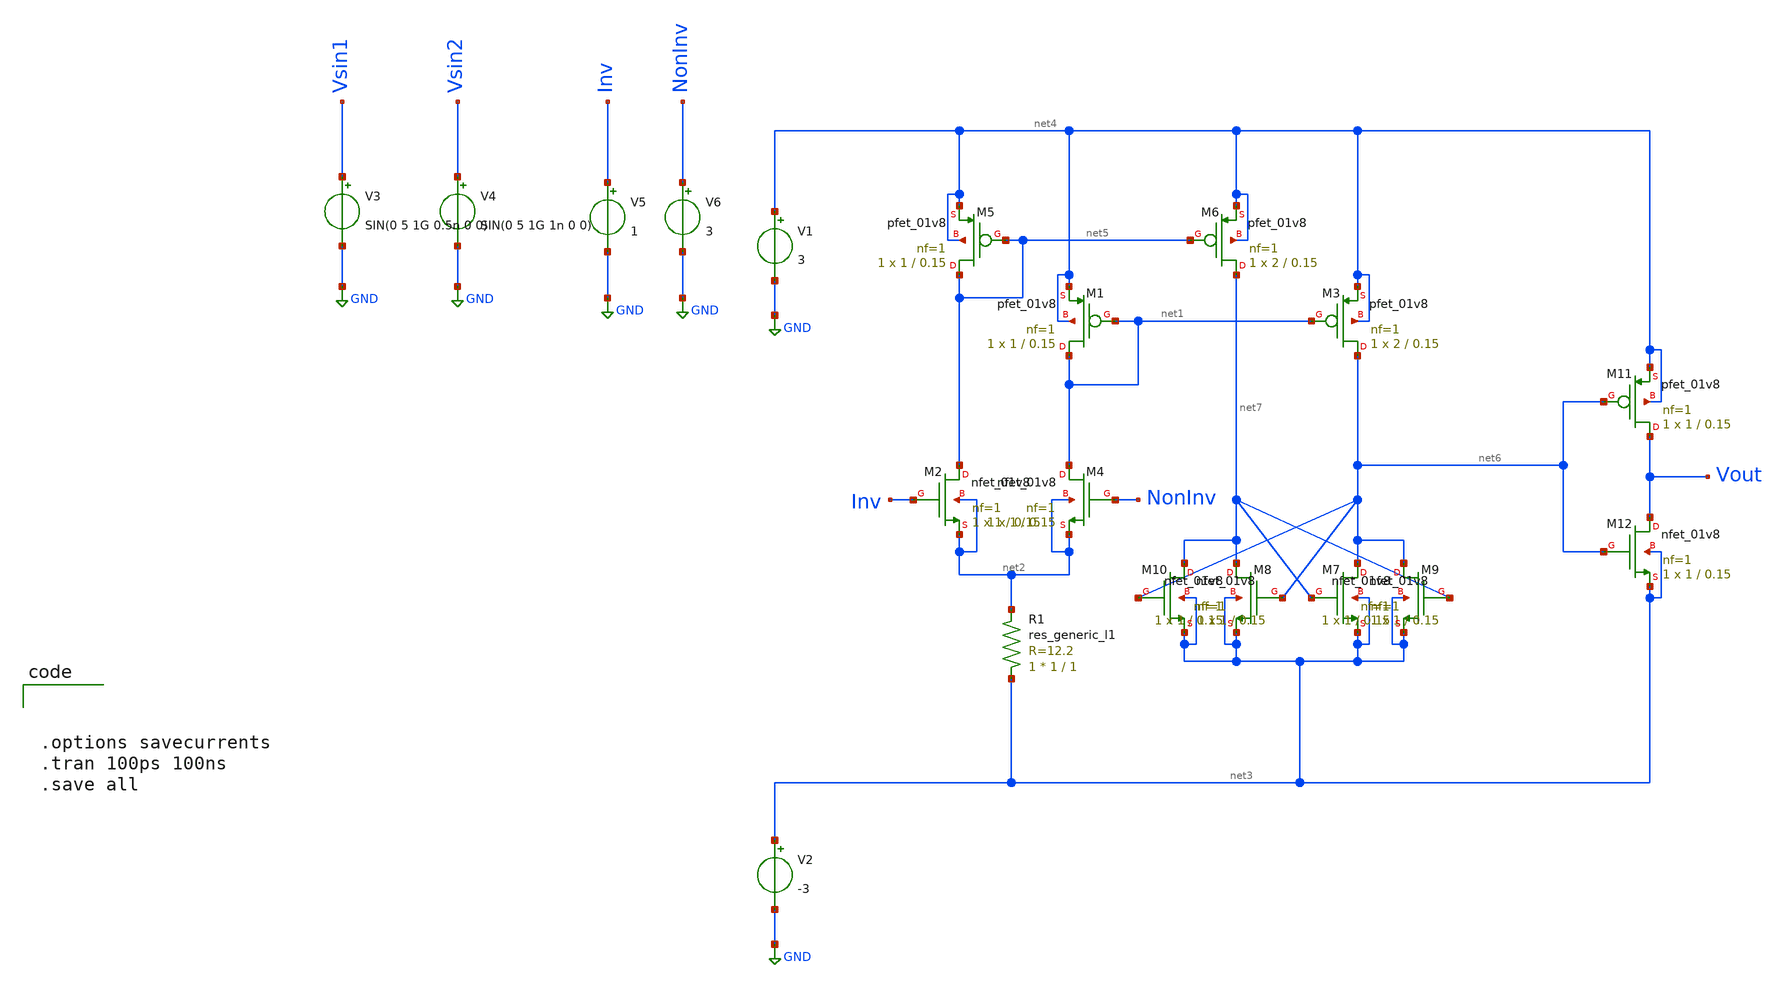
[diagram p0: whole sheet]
** sch_path: Sky130 xsch magic/xscheme/mos_comparator.sch
**.subckt mos_comparator
XM1 net1 net1 net4 net4 sky130_fd_pr__pfet_01v8 L=0.15 W=1 nf=1 ad='int((nf+1)/2) * W/nf * 0.29' as='int((nf+2)/2) * W/nf * 0.29'
+ pd='2*int((nf+1)/2) * (W/nf + 0.29)' ps='2*int((nf+2)/2) * (W/nf + 0.29)' nrd='0.29 / W' nrs='0.29 / W'
+ sa=0 sb=0 sd=0 mult=1 m=1
XM2 net5 Inv net2 net2 sky130_fd_pr__nfet_01v8 L=0.15 W=1 nf=1 ad='int((nf+1)/2) * W/nf * 0.29' as='int((nf+2)/2) * W/nf * 0.29'
+ pd='2*int((nf+1)/2) * (W/nf + 0.29)' ps='2*int((nf+2)/2) * (W/nf + 0.29)' nrd='0.29 / W' nrs='0.29 / W'
+ sa=0 sb=0 sd=0 mult=1 m=1
XM3 net6 net1 net4 net4 sky130_fd_pr__pfet_01v8 L=0.15 W=2 nf=1 ad='int((nf+1)/2) * W/nf * 0.29' as='int((nf+2)/2) * W/nf * 0.29'
+ pd='2*int((nf+1)/2) * (W/nf + 0.29)' ps='2*int((nf+2)/2) * (W/nf + 0.29)' nrd='0.29 / W' nrs='0.29 / W'
+ sa=0 sb=0 sd=0 mult=1 m=1
XM4 net1 NonInv net2 net2 sky130_fd_pr__nfet_01v8 L=0.15 W=1 nf=1 ad='int((nf+1)/2) * W/nf * 0.29' as='int((nf+2)/2) * W/nf * 0.29'
+ pd='2*int((nf+1)/2) * (W/nf + 0.29)' ps='2*int((nf+2)/2) * (W/nf + 0.29)' nrd='0.29 / W' nrs='0.29 / W'
+ sa=0 sb=0 sd=0 mult=1 m=1
R1 net3 net2 sky130_fd_pr__res_generic_l1 W=1 L=1 m=1
V1 net4 GND 3
V2 net3 GND -3
V3 Vsin1 GND SIN(0 5 1G 0.5n 0 0)
V4 Vsin2 GND SIN(0 5 1G 1n 0 0)
XM5 net5 net5 net4 net4 sky130_fd_pr__pfet_01v8 L=0.15 W=1 nf=1 ad='int((nf+1)/2) * W/nf * 0.29' as='int((nf+2)/2) * W/nf * 0.29'
+ pd='2*int((nf+1)/2) * (W/nf + 0.29)' ps='2*int((nf+2)/2) * (W/nf + 0.29)' nrd='0.29 / W' nrs='0.29 / W'
+ sa=0 sb=0 sd=0 mult=1 m=1
XM6 net7 net5 net4 net4 sky130_fd_pr__pfet_01v8 L=0.15 W=2 nf=1 ad='int((nf+1)/2) * W/nf * 0.29' as='int((nf+2)/2) * W/nf * 0.29'
+ pd='2*int((nf+1)/2) * (W/nf + 0.29)' ps='2*int((nf+2)/2) * (W/nf + 0.29)' nrd='0.29 / W' nrs='0.29 / W'
+ sa=0 sb=0 sd=0 mult=1 m=1
XM7 net6 net7 net3 net3 sky130_fd_pr__nfet_01v8 L=0.15 W=1 nf=1 ad='int((nf+1)/2) * W/nf * 0.29' as='int((nf+2)/2) * W/nf * 0.29'
+ pd='2*int((nf+1)/2) * (W/nf + 0.29)' ps='2*int((nf+2)/2) * (W/nf + 0.29)' nrd='0.29 / W' nrs='0.29 / W'
+ sa=0 sb=0 sd=0 mult=1 m=1
XM8 net7 net6 net3 net3 sky130_fd_pr__nfet_01v8 L=0.15 W=1 nf=1 ad='int((nf+1)/2) * W/nf * 0.29' as='int((nf+2)/2) * W/nf * 0.29'
+ pd='2*int((nf+1)/2) * (W/nf + 0.29)' ps='2*int((nf+2)/2) * (W/nf + 0.29)' nrd='0.29 / W' nrs='0.29 / W'
+ sa=0 sb=0 sd=0 mult=1 m=1
XM9 net6 net7 net3 net3 sky130_fd_pr__nfet_01v8 L=0.15 W=1 nf=1 ad='int((nf+1)/2) * W/nf * 0.29' as='int((nf+2)/2) * W/nf * 0.29'
+ pd='2*int((nf+1)/2) * (W/nf + 0.29)' ps='2*int((nf+2)/2) * (W/nf + 0.29)' nrd='0.29 / W' nrs='0.29 / W'
+ sa=0 sb=0 sd=0 mult=1 m=1
XM10 net7 net6 net3 net3 sky130_fd_pr__nfet_01v8 L=0.15 W=1 nf=1 ad='int((nf+1)/2) * W/nf * 0.29' as='int((nf+2)/2) * W/nf * 0.29'
+ pd='2*int((nf+1)/2) * (W/nf + 0.29)' ps='2*int((nf+2)/2) * (W/nf + 0.29)' nrd='0.29 / W' nrs='0.29 / W'
+ sa=0 sb=0 sd=0 mult=1 m=1
V5 Inv GND 1
V6 NonInv GND 3
XM11 Vout net6 net4 net4 sky130_fd_pr__pfet_01v8 L=0.15 W=1 nf=1 ad='int((nf+1)/2) * W/nf * 0.29' as='int((nf+2)/2) * W/nf * 0.29'
+ pd='2*int((nf+1)/2) * (W/nf + 0.29)' ps='2*int((nf+2)/2) * (W/nf + 0.29)' nrd='0.29 / W' nrs='0.29 / W'
+ sa=0 sb=0 sd=0 mult=1 m=1
XM12 Vout net6 net3 net3 sky130_fd_pr__nfet_01v8 L=0.15 W=1 nf=1 ad='int((nf+1)/2) * W/nf * 0.29' as='int((nf+2)/2) * W/nf * 0.29'
+ pd='2*int((nf+1)/2) * (W/nf + 0.29)' ps='2*int((nf+2)/2) * (W/nf + 0.29)' nrd='0.29 / W' nrs='0.29 / W'
+ sa=0 sb=0 sd=0 mult=1 m=1
**** begin user architecture code



.lib /usr/local/share/xschem/xschem_library/devices/sky130A/libs.tech/ngspice/sky130.lib.spice tt




.options savecurrents
.tran 100ps 100ns
.save all



**** end user architecture code
**.ends
.GLOBAL GND
.end
